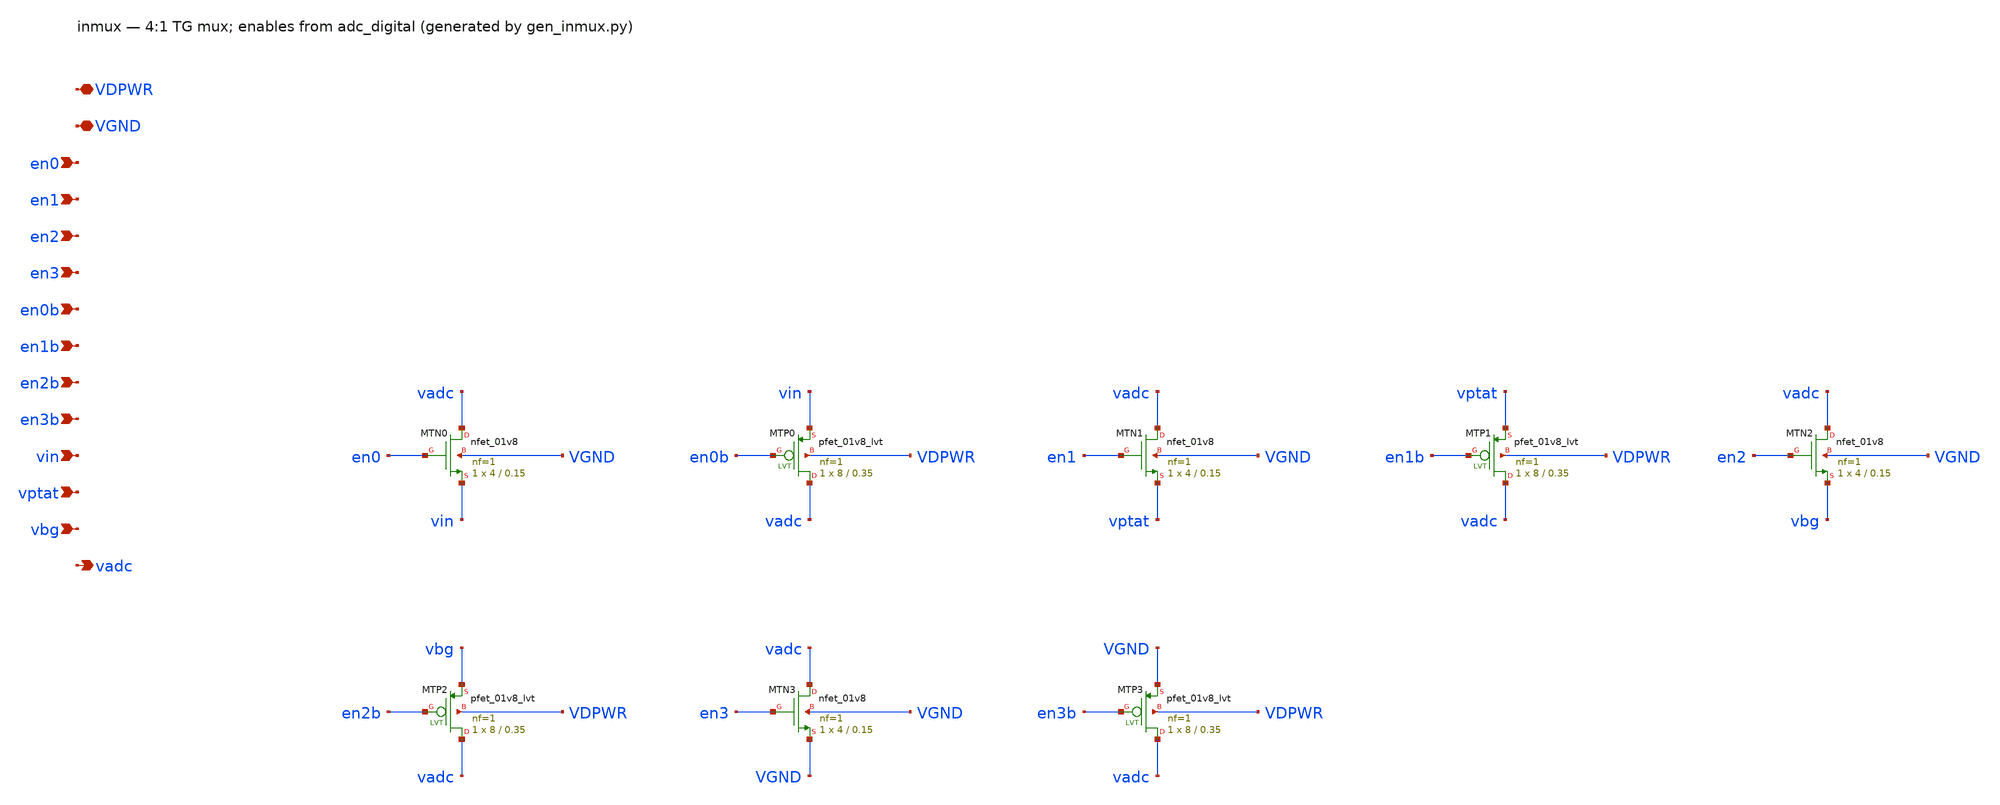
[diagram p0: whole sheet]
** sch_path: xschem/inmux.sch
**.subckt inmux VDPWR VGND en0 en1 en2 en3 en0b en1b en2b en3b vin vptat vbg vadc
*.iopin VDPWR
*.iopin VGND
*.ipin en0
*.ipin en1
*.ipin en2
*.ipin en3
*.ipin en0b
*.ipin en1b
*.ipin en2b
*.ipin en3b
*.ipin vin
*.ipin vptat
*.ipin vbg
*.opin vadc
XMTN0 vadc en0 vin VGND sky130_fd_pr__nfet_01v8 L=0.15 W=4 nf=1 ad='int((1 + 1)/2) * 4 / 1 * 0.29' as='int((1 + 2)/2) * 4 / 1 * 0.29'
+ pd='2*int((1 + 1)/2) * (4 / 1 + 0.29)' ps='2*int((1 + 2)/2) * (4 / 1 + 0.29)' nrd='0.29 / 4 ' nrs='0.29 / 4 '
+ sa=0 sb=0 sd=0 mult=1 m=1
XMTP0 vadc en0b vin VDPWR sky130_fd_pr__pfet_01v8_lvt L=0.35 W=8 nf=1 ad='int((1 + 1)/2) * 8 / 1 * 0.29'
+ as='int((1 + 2)/2) * 8 / 1 * 0.29' pd='2*int((1 + 1)/2) * (8 / 1 + 0.29)' ps='2*int((1 + 2)/2) * (8 / 1 + 0.29)'
+ nrd='0.29 / 8 ' nrs='0.29 / 8 ' sa=0 sb=0 sd=0 mult=1 m=1
XMTN1 vadc en1 vptat VGND sky130_fd_pr__nfet_01v8 L=0.15 W=4 nf=1 ad='int((1 + 1)/2) * 4 / 1 * 0.29'
+ as='int((1 + 2)/2) * 4 / 1 * 0.29' pd='2*int((1 + 1)/2) * (4 / 1 + 0.29)' ps='2*int((1 + 2)/2) * (4 / 1 + 0.29)'
+ nrd='0.29 / 4 ' nrs='0.29 / 4 ' sa=0 sb=0 sd=0 mult=1 m=1
XMTP1 vadc en1b vptat VDPWR sky130_fd_pr__pfet_01v8_lvt L=0.35 W=8 nf=1 ad='int((1 + 1)/2) * 8 / 1 * 0.29'
+ as='int((1 + 2)/2) * 8 / 1 * 0.29' pd='2*int((1 + 1)/2) * (8 / 1 + 0.29)' ps='2*int((1 + 2)/2) * (8 / 1 + 0.29)'
+ nrd='0.29 / 8 ' nrs='0.29 / 8 ' sa=0 sb=0 sd=0 mult=1 m=1
XMTN2 vadc en2 vbg VGND sky130_fd_pr__nfet_01v8 L=0.15 W=4 nf=1 ad='int((1 + 1)/2) * 4 / 1 * 0.29' as='int((1 + 2)/2) * 4 / 1 * 0.29'
+ pd='2*int((1 + 1)/2) * (4 / 1 + 0.29)' ps='2*int((1 + 2)/2) * (4 / 1 + 0.29)' nrd='0.29 / 4 ' nrs='0.29 / 4 '
+ sa=0 sb=0 sd=0 mult=1 m=1
XMTP2 vadc en2b vbg VDPWR sky130_fd_pr__pfet_01v8_lvt L=0.35 W=8 nf=1 ad='int((1 + 1)/2) * 8 / 1 * 0.29'
+ as='int((1 + 2)/2) * 8 / 1 * 0.29' pd='2*int((1 + 1)/2) * (8 / 1 + 0.29)' ps='2*int((1 + 2)/2) * (8 / 1 + 0.29)'
+ nrd='0.29 / 8 ' nrs='0.29 / 8 ' sa=0 sb=0 sd=0 mult=1 m=1
XMTN3 vadc en3 VGND VGND sky130_fd_pr__nfet_01v8 L=0.15 W=4 nf=1 ad='int((1 + 1)/2) * 4 / 1 * 0.29' as='int((1 + 2)/2) * 4 / 1 * 0.29'
+ pd='2*int((1 + 1)/2) * (4 / 1 + 0.29)' ps='2*int((1 + 2)/2) * (4 / 1 + 0.29)' nrd='0.29 / 4 ' nrs='0.29 / 4 '
+ sa=0 sb=0 sd=0 mult=1 m=1
XMTP3 vadc en3b VGND VDPWR sky130_fd_pr__pfet_01v8_lvt L=0.35 W=8 nf=1 ad='int((1 + 1)/2) * 8 / 1 * 0.29'
+ as='int((1 + 2)/2) * 8 / 1 * 0.29' pd='2*int((1 + 1)/2) * (8 / 1 + 0.29)' ps='2*int((1 + 2)/2) * (8 / 1 + 0.29)'
+ nrd='0.29 / 8 ' nrs='0.29 / 8 ' sa=0 sb=0 sd=0 mult=1 m=1
**.ends
.end
